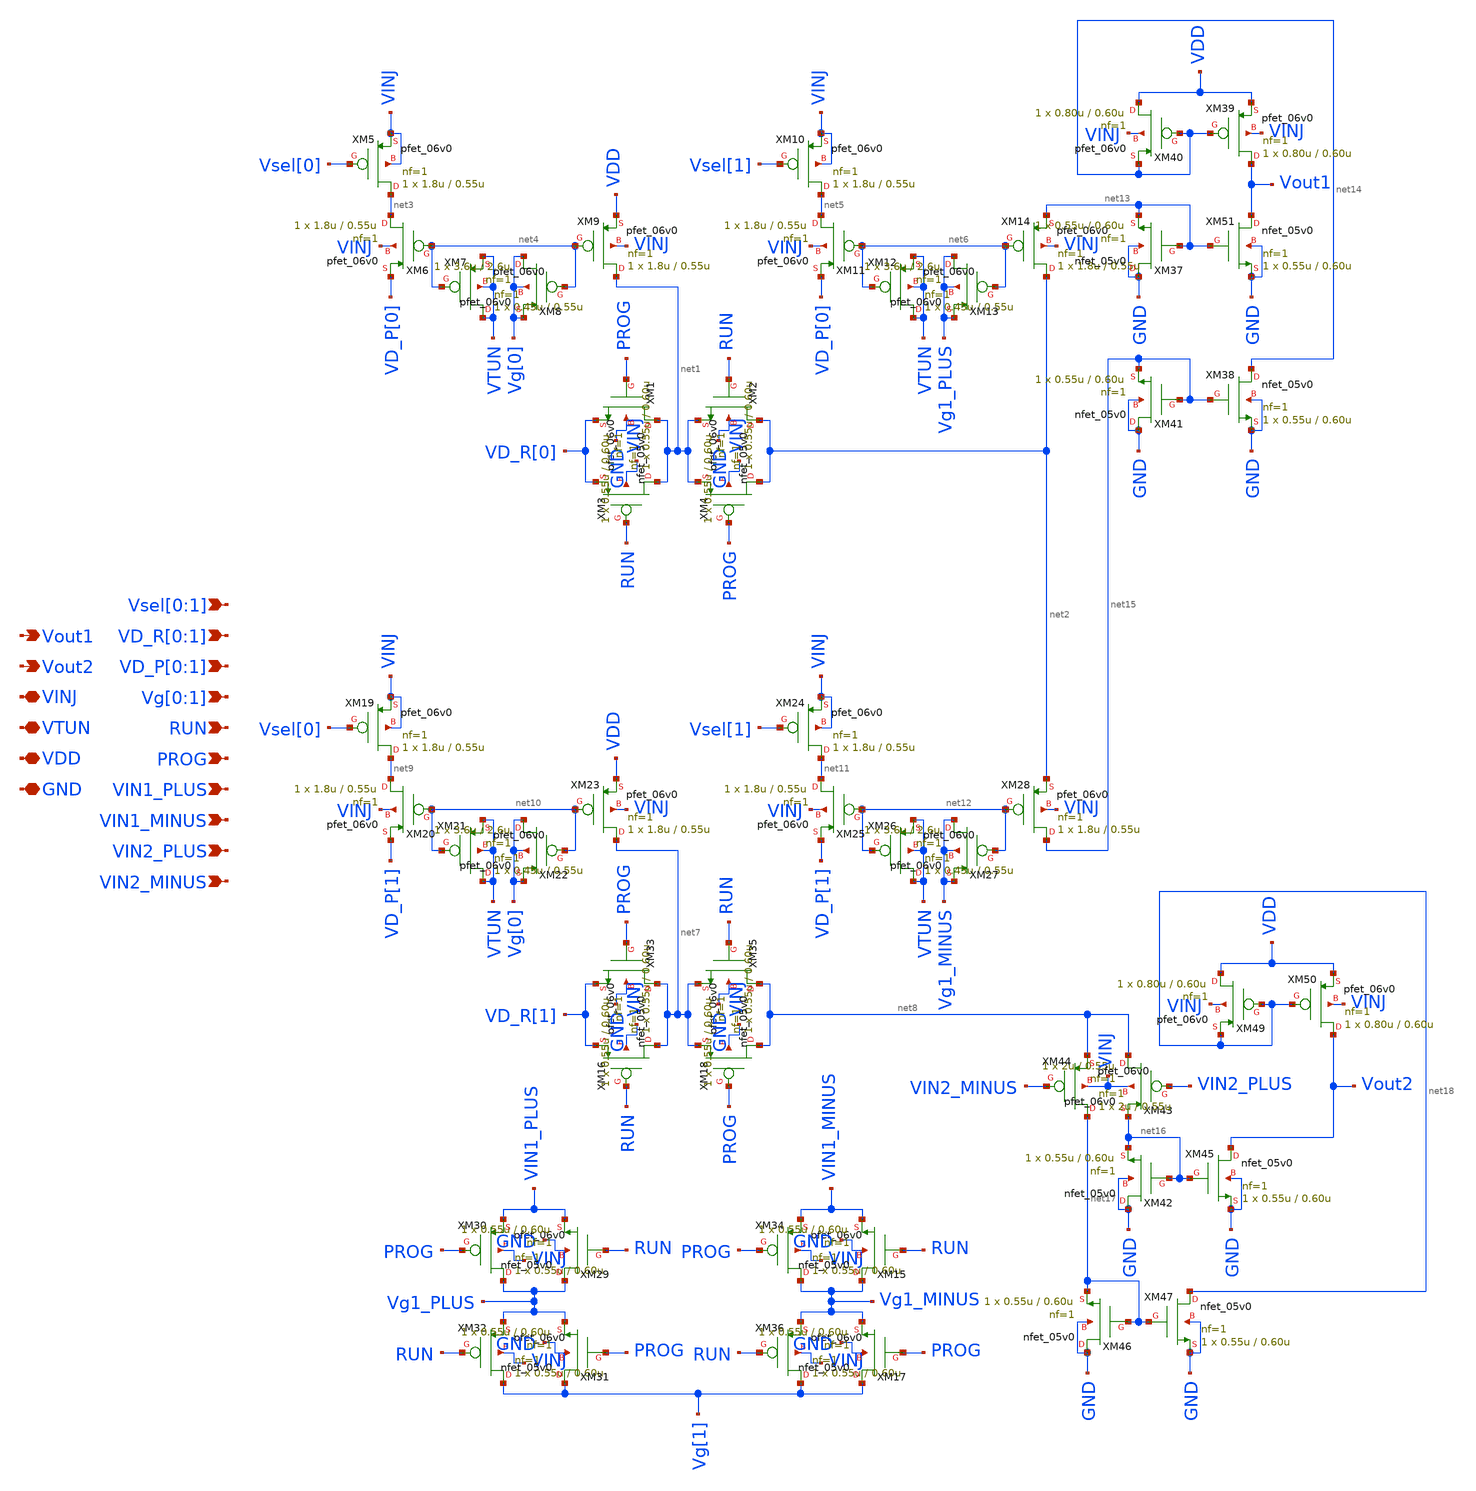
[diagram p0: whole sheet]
** sch_path: 1_Design/GF180_cells/2TA/gf180_2TA_1FG_Strong.sch
**.subckt gf180_2TA_1FG_Strong Vsel[0],Vsel[1] Vout1 VINJ VTUN Vout2 VDD GND VD_R[0],VD_R[1]
*+ VD_P[0],VD_P[1] Vg[0],Vg[1] RUN PROG VIN1_PLUS VIN1_MINUS VIN2_PLUS VIN2_MINUS
*.ipin Vsel[0],Vsel[1]
*.opin Vout1
*.iopin VINJ
*.iopin VTUN
*.opin Vout2
*.iopin VDD
*.iopin GND
*.ipin VD_R[0],VD_R[1]
*.ipin VD_P[0],VD_P[1]
*.ipin Vg[0],Vg[1]
*.ipin RUN
*.ipin PROG
*.ipin VIN1_PLUS
*.ipin VIN1_MINUS
*.ipin VIN2_PLUS
*.ipin VIN2_MINUS
XM3 net1 RUN VD_R[0] VINJ pfet_06v0 L=0.60u W=0.55u nf=1 ad='int((nf+1)/2) * W/nf * 0.18u' as='int((nf+2)/2) * W/nf * 0.18u'
+ pd='2*int((nf+1)/2) * (W/nf + 0.18u)' ps='2*int((nf+2)/2) * (W/nf + 0.18u)' nrd='0.18u / W' nrs='0.18u / W'
+ sa=0 sb=0 sd=0 m=1
XM4 net2 PROG net1 VINJ pfet_06v0 L=0.60u W=0.55u nf=1 ad='int((nf+1)/2) * W/nf * 0.18u' as='int((nf+2)/2) * W/nf * 0.18u'
+ pd='2*int((nf+1)/2) * (W/nf + 0.18u)' ps='2*int((nf+2)/2) * (W/nf + 0.18u)' nrd='0.18u / W' nrs='0.18u / W'
+ sa=0 sb=0 sd=0 m=1
XM5 net3 Vsel[0] VINJ VINJ pfet_06v0 L=0.55u W=1.8u nf=1 ad='int((nf+1)/2) * W/nf * 0.18u' as='int((nf+2)/2) * W/nf * 0.18u'
+ pd='2*int((nf+1)/2) * (W/nf + 0.18u)' ps='2*int((nf+2)/2) * (W/nf + 0.18u)' nrd='0.18u / W' nrs='0.18u / W'
+ sa=0 sb=0 sd=0 m=1
XM6 net3 net4 VD_P[0] VINJ pfet_06v0 L=0.55u W=1.8u nf=1 ad='int((nf+1)/2) * W/nf * 0.18u' as='int((nf+2)/2) * W/nf * 0.18u'
+ pd='2*int((nf+1)/2) * (W/nf + 0.18u)' ps='2*int((nf+2)/2) * (W/nf + 0.18u)' nrd='0.18u / W' nrs='0.18u / W'
+ sa=0 sb=0 sd=0 m=1
XM7 VTUN net4 VTUN VTUN pfet_06v0 L=0.55u W=0.45u nf=1 ad='int((nf+1)/2) * W/nf * 0.18u' as='int((nf+2)/2) * W/nf * 0.18u'
+ pd='2*int((nf+1)/2) * (W/nf + 0.18u)' ps='2*int((nf+2)/2) * (W/nf + 0.18u)' nrd='0.18u / W' nrs='0.18u / W'
+ sa=0 sb=0 sd=0 m=1
XM8 Vg[0] net4 Vg[0] Vg[0] pfet_06v0 L=2.6u W=3.6u nf=1 ad='int((nf+1)/2) * W/nf * 0.18u' as='int((nf+2)/2) * W/nf * 0.18u'
+ pd='2*int((nf+1)/2) * (W/nf + 0.18u)' ps='2*int((nf+2)/2) * (W/nf + 0.18u)' nrd='0.18u / W' nrs='0.18u / W'
+ sa=0 sb=0 sd=0 m=1
XM9 net1 net4 VDD VINJ pfet_06v0 L=0.55u W=1.8u nf=1 ad='int((nf+1)/2) * W/nf * 0.18u' as='int((nf+2)/2) * W/nf * 0.18u'
+ pd='2*int((nf+1)/2) * (W/nf + 0.18u)' ps='2*int((nf+2)/2) * (W/nf + 0.18u)' nrd='0.18u / W' nrs='0.18u / W'
+ sa=0 sb=0 sd=0 m=1
XM10 net5 Vsel[1] VINJ VINJ pfet_06v0 L=0.55u W=1.8u nf=1 ad='int((nf+1)/2) * W/nf * 0.18u' as='int((nf+2)/2) * W/nf * 0.18u'
+ pd='2*int((nf+1)/2) * (W/nf + 0.18u)' ps='2*int((nf+2)/2) * (W/nf + 0.18u)' nrd='0.18u / W' nrs='0.18u / W'
+ sa=0 sb=0 sd=0 m=1
XM11 net5 net6 VD_P[0] VINJ pfet_06v0 L=0.55u W=1.8u nf=1 ad='int((nf+1)/2) * W/nf * 0.18u' as='int((nf+2)/2) * W/nf * 0.18u'
+ pd='2*int((nf+1)/2) * (W/nf + 0.18u)' ps='2*int((nf+2)/2) * (W/nf + 0.18u)' nrd='0.18u / W' nrs='0.18u / W'
+ sa=0 sb=0 sd=0 m=1
XM12 VTUN net6 VTUN VTUN pfet_06v0 L=0.55u W=0.45u nf=1 ad='int((nf+1)/2) * W/nf * 0.18u' as='int((nf+2)/2) * W/nf * 0.18u'
+ pd='2*int((nf+1)/2) * (W/nf + 0.18u)' ps='2*int((nf+2)/2) * (W/nf + 0.18u)' nrd='0.18u / W' nrs='0.18u / W'
+ sa=0 sb=0 sd=0 m=1
XM13 Vg1_PLUS net6 Vg1_PLUS Vg1_PLUS pfet_06v0 L=2.6u W=3.6u nf=1 ad='int((nf+1)/2) * W/nf * 0.18u' as='int((nf+2)/2) * W/nf * 0.18u'
+ pd='2*int((nf+1)/2) * (W/nf + 0.18u)' ps='2*int((nf+2)/2) * (W/nf + 0.18u)' nrd='0.18u / W' nrs='0.18u / W'
+ sa=0 sb=0 sd=0 m=1
XM14 net2 net6 net13 VINJ pfet_06v0 L=0.55u W=1.8u nf=1 ad='int((nf+1)/2) * W/nf * 0.18u' as='int((nf+2)/2) * W/nf * 0.18u'
+ pd='2*int((nf+1)/2) * (W/nf + 0.18u)' ps='2*int((nf+2)/2) * (W/nf + 0.18u)' nrd='0.18u / W' nrs='0.18u / W'
+ sa=0 sb=0 sd=0 m=1
XM16 net7 RUN VD_R[1] VINJ pfet_06v0 L=0.60u W=0.55u nf=1 ad='int((nf+1)/2) * W/nf * 0.18u' as='int((nf+2)/2) * W/nf * 0.18u'
+ pd='2*int((nf+1)/2) * (W/nf + 0.18u)' ps='2*int((nf+2)/2) * (W/nf + 0.18u)' nrd='0.18u / W' nrs='0.18u / W'
+ sa=0 sb=0 sd=0 m=1
XM18 net8 PROG net7 VINJ pfet_06v0 L=0.60u W=0.55u nf=1 ad='int((nf+1)/2) * W/nf * 0.18u' as='int((nf+2)/2) * W/nf * 0.18u'
+ pd='2*int((nf+1)/2) * (W/nf + 0.18u)' ps='2*int((nf+2)/2) * (W/nf + 0.18u)' nrd='0.18u / W' nrs='0.18u / W'
+ sa=0 sb=0 sd=0 m=1
XM19 net9 Vsel[0] VINJ VINJ pfet_06v0 L=0.55u W=1.8u nf=1 ad='int((nf+1)/2) * W/nf * 0.18u' as='int((nf+2)/2) * W/nf * 0.18u'
+ pd='2*int((nf+1)/2) * (W/nf + 0.18u)' ps='2*int((nf+2)/2) * (W/nf + 0.18u)' nrd='0.18u / W' nrs='0.18u / W'
+ sa=0 sb=0 sd=0 m=1
XM20 net9 net10 VD_P[1] VINJ pfet_06v0 L=0.55u W=1.8u nf=1 ad='int((nf+1)/2) * W/nf * 0.18u' as='int((nf+2)/2) * W/nf * 0.18u'
+ pd='2*int((nf+1)/2) * (W/nf + 0.18u)' ps='2*int((nf+2)/2) * (W/nf + 0.18u)' nrd='0.18u / W' nrs='0.18u / W'
+ sa=0 sb=0 sd=0 m=1
XM21 VTUN net10 VTUN VTUN pfet_06v0 L=0.55u W=0.45u nf=1 ad='int((nf+1)/2) * W/nf * 0.18u' as='int((nf+2)/2) * W/nf * 0.18u'
+ pd='2*int((nf+1)/2) * (W/nf + 0.18u)' ps='2*int((nf+2)/2) * (W/nf + 0.18u)' nrd='0.18u / W' nrs='0.18u / W'
+ sa=0 sb=0 sd=0 m=1
XM22 Vg[0] net10 Vg[0] Vg[0] pfet_06v0 L=2.6u W=3.6u nf=1 ad='int((nf+1)/2) * W/nf * 0.18u' as='int((nf+2)/2) * W/nf * 0.18u'
+ pd='2*int((nf+1)/2) * (W/nf + 0.18u)' ps='2*int((nf+2)/2) * (W/nf + 0.18u)' nrd='0.18u / W' nrs='0.18u / W'
+ sa=0 sb=0 sd=0 m=1
XM23 net7 net10 VDD VINJ pfet_06v0 L=0.55u W=1.8u nf=1 ad='int((nf+1)/2) * W/nf * 0.18u' as='int((nf+2)/2) * W/nf * 0.18u'
+ pd='2*int((nf+1)/2) * (W/nf + 0.18u)' ps='2*int((nf+2)/2) * (W/nf + 0.18u)' nrd='0.18u / W' nrs='0.18u / W'
+ sa=0 sb=0 sd=0 m=1
XM24 net11 Vsel[1] VINJ VINJ pfet_06v0 L=0.55u W=1.8u nf=1 ad='int((nf+1)/2) * W/nf * 0.18u' as='int((nf+2)/2) * W/nf * 0.18u'
+ pd='2*int((nf+1)/2) * (W/nf + 0.18u)' ps='2*int((nf+2)/2) * (W/nf + 0.18u)' nrd='0.18u / W' nrs='0.18u / W'
+ sa=0 sb=0 sd=0 m=1
XM25 net11 net12 VD_P[1] VINJ pfet_06v0 L=0.55u W=1.8u nf=1 ad='int((nf+1)/2) * W/nf * 0.18u' as='int((nf+2)/2) * W/nf * 0.18u'
+ pd='2*int((nf+1)/2) * (W/nf + 0.18u)' ps='2*int((nf+2)/2) * (W/nf + 0.18u)' nrd='0.18u / W' nrs='0.18u / W'
+ sa=0 sb=0 sd=0 m=1
XM26 VTUN net12 VTUN VTUN pfet_06v0 L=0.55u W=0.45u nf=1 ad='int((nf+1)/2) * W/nf * 0.18u' as='int((nf+2)/2) * W/nf * 0.18u'
+ pd='2*int((nf+1)/2) * (W/nf + 0.18u)' ps='2*int((nf+2)/2) * (W/nf + 0.18u)' nrd='0.18u / W' nrs='0.18u / W'
+ sa=0 sb=0 sd=0 m=1
XM27 Vg1_MINUS net12 Vg1_MINUS Vg1_MINUS pfet_06v0 L=2.6u W=3.6u nf=1 ad='int((nf+1)/2) * W/nf * 0.18u'
+ as='int((nf+2)/2) * W/nf * 0.18u' pd='2*int((nf+1)/2) * (W/nf + 0.18u)' ps='2*int((nf+2)/2) * (W/nf + 0.18u)'
+ nrd='0.18u / W' nrs='0.18u / W' sa=0 sb=0 sd=0 m=1
XM28 net15 net12 net2 VINJ pfet_06v0 L=0.55u W=1.8u nf=1 ad='int((nf+1)/2) * W/nf * 0.18u' as='int((nf+2)/2) * W/nf * 0.18u'
+ pd='2*int((nf+1)/2) * (W/nf + 0.18u)' ps='2*int((nf+2)/2) * (W/nf + 0.18u)' nrd='0.18u / W' nrs='0.18u / W'
+ sa=0 sb=0 sd=0 m=1
XM30 Vg1_PLUS PROG VIN1_PLUS VINJ pfet_06v0 L=0.60u W=0.55u nf=1 ad='int((nf+1)/2) * W/nf * 0.18u' as='int((nf+2)/2) * W/nf * 0.18u'
+ pd='2*int((nf+1)/2) * (W/nf + 0.18u)' ps='2*int((nf+2)/2) * (W/nf + 0.18u)' nrd='0.18u / W' nrs='0.18u / W'
+ sa=0 sb=0 sd=0 m=1
XM32 Vg[1] RUN Vg1_PLUS VINJ pfet_06v0 L=0.60u W=0.55u nf=1 ad='int((nf+1)/2) * W/nf * 0.18u' as='int((nf+2)/2) * W/nf * 0.18u'
+ pd='2*int((nf+1)/2) * (W/nf + 0.18u)' ps='2*int((nf+2)/2) * (W/nf + 0.18u)' nrd='0.18u / W' nrs='0.18u / W'
+ sa=0 sb=0 sd=0 m=1
XM34 Vg1_MINUS PROG VIN1_MINUS VINJ pfet_06v0 L=0.60u W=0.55u nf=1 ad='int((nf+1)/2) * W/nf * 0.18u'
+ as='int((nf+2)/2) * W/nf * 0.18u' pd='2*int((nf+1)/2) * (W/nf + 0.18u)' ps='2*int((nf+2)/2) * (W/nf + 0.18u)'
+ nrd='0.18u / W' nrs='0.18u / W' sa=0 sb=0 sd=0 m=1
XM36 Vg[1] RUN Vg1_MINUS VINJ pfet_06v0 L=0.60u W=0.55u nf=1 ad='int((nf+1)/2) * W/nf * 0.18u' as='int((nf+2)/2) * W/nf * 0.18u'
+ pd='2*int((nf+1)/2) * (W/nf + 0.18u)' ps='2*int((nf+2)/2) * (W/nf + 0.18u)' nrd='0.18u / W' nrs='0.18u / W'
+ sa=0 sb=0 sd=0 m=1
XM39 Vout1 net14 VDD VINJ pfet_06v0 L=0.60u W=0.80u nf=1 ad='int((nf+1)/2) * W/nf * 0.18u' as='int((nf+2)/2) * W/nf * 0.18u'
+ pd='2*int((nf+1)/2) * (W/nf + 0.18u)' ps='2*int((nf+2)/2) * (W/nf + 0.18u)' nrd='0.18u / W' nrs='0.18u / W'
+ sa=0 sb=0 sd=0 m=1
XM40 VDD net14 net14 VINJ pfet_06v0 L=0.60u W=0.80u nf=1 ad='int((nf+1)/2) * W/nf * 0.18u' as='int((nf+2)/2) * W/nf * 0.18u'
+ pd='2*int((nf+1)/2) * (W/nf + 0.18u)' ps='2*int((nf+2)/2) * (W/nf + 0.18u)' nrd='0.18u / W' nrs='0.18u / W'
+ sa=0 sb=0 sd=0 m=1
XM43 net8 VIN2_PLUS net16 VINJ pfet_06v0 L=0.55u W=2u nf=1 ad='int((nf+1)/2) * W/nf * 0.18u' as='int((nf+2)/2) * W/nf * 0.18u'
+ pd='2*int((nf+1)/2) * (W/nf + 0.18u)' ps='2*int((nf+2)/2) * (W/nf + 0.18u)' nrd='0.18u / W' nrs='0.18u / W'
+ sa=0 sb=0 sd=0 m=1
XM44 net17 VIN2_MINUS net8 VINJ pfet_06v0 L=0.55u W=2u nf=1 ad='int((nf+1)/2) * W/nf * 0.18u' as='int((nf+2)/2) * W/nf * 0.18u'
+ pd='2*int((nf+1)/2) * (W/nf + 0.18u)' ps='2*int((nf+2)/2) * (W/nf + 0.18u)' nrd='0.18u / W' nrs='0.18u / W'
+ sa=0 sb=0 sd=0 m=1
XM49 VDD net18 net18 VINJ pfet_06v0 L=0.60u W=0.80u nf=1 ad='int((nf+1)/2) * W/nf * 0.18u' as='int((nf+2)/2) * W/nf * 0.18u'
+ pd='2*int((nf+1)/2) * (W/nf + 0.18u)' ps='2*int((nf+2)/2) * (W/nf + 0.18u)' nrd='0.18u / W' nrs='0.18u / W'
+ sa=0 sb=0 sd=0 m=1
XM50 Vout2 net18 VDD VINJ pfet_06v0 L=0.60u W=0.80u nf=1 ad='int((nf+1)/2) * W/nf * 0.18u' as='int((nf+2)/2) * W/nf * 0.18u'
+ pd='2*int((nf+1)/2) * (W/nf + 0.18u)' ps='2*int((nf+2)/2) * (W/nf + 0.18u)' nrd='0.18u / W' nrs='0.18u / W'
+ sa=0 sb=0 sd=0 m=1
XM51 Vout1 net13 GND GND nfet_05v0 L=0.60u W=0.55u nf=1 ad='int((nf+1)/2) * W/nf * 0.18u' as='int((nf+2)/2) * W/nf * 0.18u'
+ pd='2*int((nf+1)/2) * (W/nf + 0.18u)' ps='2*int((nf+2)/2) * (W/nf + 0.18u)' nrd='0.18u / W' nrs='0.18u / W'
+ sa=0 sb=0 sd=0 m=1
XM37 GND net13 net13 GND nfet_05v0 L=0.60u W=0.55u nf=1 ad='int((nf+1)/2) * W/nf * 0.18u' as='int((nf+2)/2) * W/nf * 0.18u'
+ pd='2*int((nf+1)/2) * (W/nf + 0.18u)' ps='2*int((nf+2)/2) * (W/nf + 0.18u)' nrd='0.18u / W' nrs='0.18u / W'
+ sa=0 sb=0 sd=0 m=1
XM38 net14 net15 GND GND nfet_05v0 L=0.60u W=0.55u nf=1 ad='int((nf+1)/2) * W/nf * 0.18u' as='int((nf+2)/2) * W/nf * 0.18u'
+ pd='2*int((nf+1)/2) * (W/nf + 0.18u)' ps='2*int((nf+2)/2) * (W/nf + 0.18u)' nrd='0.18u / W' nrs='0.18u / W'
+ sa=0 sb=0 sd=0 m=1
XM41 GND net15 net15 GND nfet_05v0 L=0.60u W=0.55u nf=1 ad='int((nf+1)/2) * W/nf * 0.18u' as='int((nf+2)/2) * W/nf * 0.18u'
+ pd='2*int((nf+1)/2) * (W/nf + 0.18u)' ps='2*int((nf+2)/2) * (W/nf + 0.18u)' nrd='0.18u / W' nrs='0.18u / W'
+ sa=0 sb=0 sd=0 m=1
XM42 GND net16 net16 GND nfet_05v0 L=0.60u W=0.55u nf=1 ad='int((nf+1)/2) * W/nf * 0.18u' as='int((nf+2)/2) * W/nf * 0.18u'
+ pd='2*int((nf+1)/2) * (W/nf + 0.18u)' ps='2*int((nf+2)/2) * (W/nf + 0.18u)' nrd='0.18u / W' nrs='0.18u / W'
+ sa=0 sb=0 sd=0 m=1
XM45 Vout2 net16 GND GND nfet_05v0 L=0.60u W=0.55u nf=1 ad='int((nf+1)/2) * W/nf * 0.18u' as='int((nf+2)/2) * W/nf * 0.18u'
+ pd='2*int((nf+1)/2) * (W/nf + 0.18u)' ps='2*int((nf+2)/2) * (W/nf + 0.18u)' nrd='0.18u / W' nrs='0.18u / W'
+ sa=0 sb=0 sd=0 m=1
XM46 GND net17 net17 GND nfet_05v0 L=0.60u W=0.55u nf=1 ad='int((nf+1)/2) * W/nf * 0.18u' as='int((nf+2)/2) * W/nf * 0.18u'
+ pd='2*int((nf+1)/2) * (W/nf + 0.18u)' ps='2*int((nf+2)/2) * (W/nf + 0.18u)' nrd='0.18u / W' nrs='0.18u / W'
+ sa=0 sb=0 sd=0 m=1
XM47 net18 net17 GND GND nfet_05v0 L=0.60u W=0.55u nf=1 ad='int((nf+1)/2) * W/nf * 0.18u' as='int((nf+2)/2) * W/nf * 0.18u'
+ pd='2*int((nf+1)/2) * (W/nf + 0.18u)' ps='2*int((nf+2)/2) * (W/nf + 0.18u)' nrd='0.18u / W' nrs='0.18u / W'
+ sa=0 sb=0 sd=0 m=1
XM15 Vg1_MINUS RUN VIN1_MINUS GND nfet_05v0 L=0.60u W=0.55u nf=1 ad='int((nf+1)/2) * W/nf * 0.18u' as='int((nf+2)/2) * W/nf * 0.18u'
+ pd='2*int((nf+1)/2) * (W/nf + 0.18u)' ps='2*int((nf+2)/2) * (W/nf + 0.18u)' nrd='0.18u / W' nrs='0.18u / W'
+ sa=0 sb=0 sd=0 m=1
XM17 Vg[1] PROG Vg1_MINUS GND nfet_05v0 L=0.60u W=0.55u nf=1 ad='int((nf+1)/2) * W/nf * 0.18u' as='int((nf+2)/2) * W/nf * 0.18u'
+ pd='2*int((nf+1)/2) * (W/nf + 0.18u)' ps='2*int((nf+2)/2) * (W/nf + 0.18u)' nrd='0.18u / W' nrs='0.18u / W'
+ sa=0 sb=0 sd=0 m=1
XM29 Vg1_PLUS RUN VIN1_PLUS GND nfet_05v0 L=0.60u W=0.55u nf=1 ad='int((nf+1)/2) * W/nf * 0.18u' as='int((nf+2)/2) * W/nf * 0.18u'
+ pd='2*int((nf+1)/2) * (W/nf + 0.18u)' ps='2*int((nf+2)/2) * (W/nf + 0.18u)' nrd='0.18u / W' nrs='0.18u / W'
+ sa=0 sb=0 sd=0 m=1
XM31 Vg[1] PROG Vg1_PLUS GND nfet_05v0 L=0.60u W=0.55u nf=1 ad='int((nf+1)/2) * W/nf * 0.18u' as='int((nf+2)/2) * W/nf * 0.18u'
+ pd='2*int((nf+1)/2) * (W/nf + 0.18u)' ps='2*int((nf+2)/2) * (W/nf + 0.18u)' nrd='0.18u / W' nrs='0.18u / W'
+ sa=0 sb=0 sd=0 m=1
XM33 net7 PROG VD_R[1] GND nfet_05v0 L=0.60u W=0.55u nf=1 ad='int((nf+1)/2) * W/nf * 0.18u' as='int((nf+2)/2) * W/nf * 0.18u'
+ pd='2*int((nf+1)/2) * (W/nf + 0.18u)' ps='2*int((nf+2)/2) * (W/nf + 0.18u)' nrd='0.18u / W' nrs='0.18u / W'
+ sa=0 sb=0 sd=0 m=1
XM35 net8 RUN net7 GND nfet_05v0 L=0.60u W=0.55u nf=1 ad='int((nf+1)/2) * W/nf * 0.18u' as='int((nf+2)/2) * W/nf * 0.18u'
+ pd='2*int((nf+1)/2) * (W/nf + 0.18u)' ps='2*int((nf+2)/2) * (W/nf + 0.18u)' nrd='0.18u / W' nrs='0.18u / W'
+ sa=0 sb=0 sd=0 m=1
XM1 net1 PROG VD_R[0] GND nfet_05v0 L=0.60u W=0.55u nf=1 ad='int((nf+1)/2) * W/nf * 0.18u' as='int((nf+2)/2) * W/nf * 0.18u'
+ pd='2*int((nf+1)/2) * (W/nf + 0.18u)' ps='2*int((nf+2)/2) * (W/nf + 0.18u)' nrd='0.18u / W' nrs='0.18u / W'
+ sa=0 sb=0 sd=0 m=1
XM2 net2 RUN net1 GND nfet_05v0 L=0.60u W=0.55u nf=1 ad='int((nf+1)/2) * W/nf * 0.18u' as='int((nf+2)/2) * W/nf * 0.18u'
+ pd='2*int((nf+1)/2) * (W/nf + 0.18u)' ps='2*int((nf+2)/2) * (W/nf + 0.18u)' nrd='0.18u / W' nrs='0.18u / W'
+ sa=0 sb=0 sd=0 m=1
**.ends
.end
